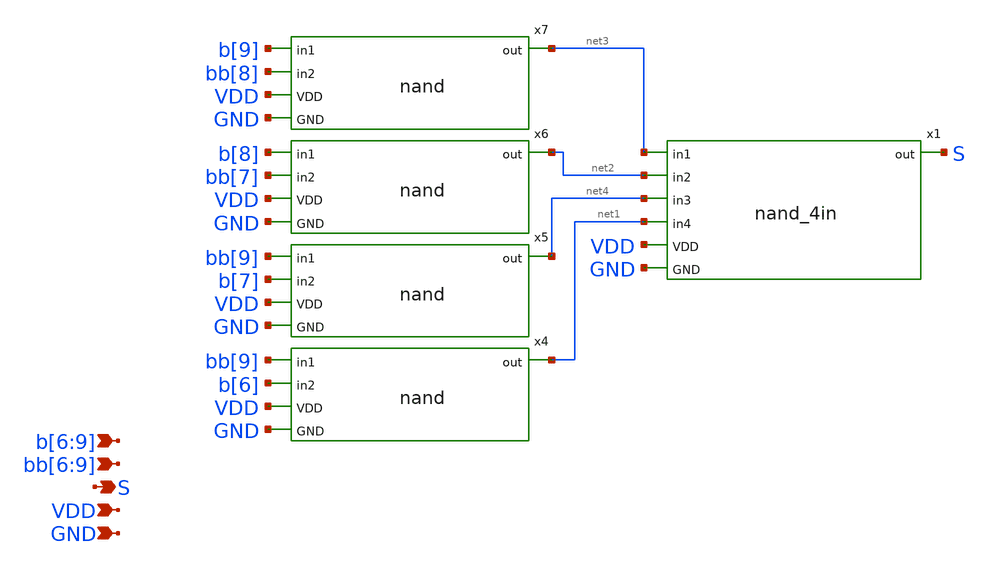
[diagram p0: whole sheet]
** sch_path: xschem/seg_selector_2_logic.sch
**.subckt seg_selector_2_logic b[6],b[7],b[8],b[9] S GND VDD bb[6],bb[7],bb[8],bb[9]
*.ipin b[6],b[7],b[8],b[9]
*.opin S
*.ipin GND
*.ipin VDD
*.ipin bb[6],bb[7],bb[8],bb[9]
x4 bb[9] b[6] net1 VDD GND nand
x5 bb[9] b[7] net4 VDD GND nand
x6 b[8] bb[7] net2 VDD GND nand
x7 b[9] bb[8] net3 VDD GND nand
x1 net3 net2 net4 net1 S VDD GND nand_4in
**.ends

* expanding   symbol:  nand.sym # of pins=5
** sym_path: xschem/nand.sym
** sch_path: xschem/nand.sch
.subckt nand in1 in2 out VDD GND
*.ipin in2
*.opin out
*.ipin VDD
*.ipin GND
*.ipin in1
.param wp=0.63 wn=0.42 l=0.15
XM1 out in1 VDD VDD sky130_fd_pr__pfet_01v8 L=l W=wp nf=1 ad='int((nf+1)/2) * W/nf * 0.29' as='int((nf+2)/2) * W/nf * 0.29'
+ pd='2*int((nf+1)/2) * (W/nf + 0.29)' ps='2*int((nf+2)/2) * (W/nf + 0.29)' nrd='0.29 / W' nrs='0.29 / W'
+ sa=0 sb=0 sd=0 mult=1 m=1
XM2 out in2 VDD VDD sky130_fd_pr__pfet_01v8 L=l W=wp nf=1 ad='int((nf+1)/2) * W/nf * 0.29' as='int((nf+2)/2) * W/nf * 0.29'
+ pd='2*int((nf+1)/2) * (W/nf + 0.29)' ps='2*int((nf+2)/2) * (W/nf + 0.29)' nrd='0.29 / W' nrs='0.29 / W'
+ sa=0 sb=0 sd=0 mult=1 m=1
XM3 out in2 net1 GND sky130_fd_pr__nfet_01v8 L=l W=wn nf=1 ad='int((nf+1)/2) * W/nf * 0.29' as='int((nf+2)/2) * W/nf * 0.29'
+ pd='2*int((nf+1)/2) * (W/nf + 0.29)' ps='2*int((nf+2)/2) * (W/nf + 0.29)' nrd='0.29 / W' nrs='0.29 / W'
+ sa=0 sb=0 sd=0 mult=1 m=1
XM4 net1 in1 GND GND sky130_fd_pr__nfet_01v8 L=l W=wn nf=1 ad='int((nf+1)/2) * W/nf * 0.29' as='int((nf+2)/2) * W/nf * 0.29'
+ pd='2*int((nf+1)/2) * (W/nf + 0.29)' ps='2*int((nf+2)/2) * (W/nf + 0.29)' nrd='0.29 / W' nrs='0.29 / W'
+ sa=0 sb=0 sd=0 mult=1 m=1
.ends


* expanding   symbol:  nand_4in.sym # of pins=7
** sym_path: xschem/nand_4in.sym
** sch_path: xschem/nand_4in.sch
.subckt nand_4in in1 in2 in3 in4 out VDD GND
*.ipin in2
*.opin out
*.ipin VDD
*.ipin GND
*.ipin in1
*.ipin in4
*.ipin in3
.param wp=0.42 wn=0.42 l=0.15
XM1 out in1 VDD VDD sky130_fd_pr__pfet_01v8 L=l W=wp nf=1 ad='int((nf+1)/2) * W/nf * 0.29' as='int((nf+2)/2) * W/nf * 0.29'
+ pd='2*int((nf+1)/2) * (W/nf + 0.29)' ps='2*int((nf+2)/2) * (W/nf + 0.29)' nrd='0.29 / W' nrs='0.29 / W'
+ sa=0 sb=0 sd=0 mult=1 m=1
XM2 out in2 VDD VDD sky130_fd_pr__pfet_01v8 L=l W=wp nf=1 ad='int((nf+1)/2) * W/nf * 0.29' as='int((nf+2)/2) * W/nf * 0.29'
+ pd='2*int((nf+1)/2) * (W/nf + 0.29)' ps='2*int((nf+2)/2) * (W/nf + 0.29)' nrd='0.29 / W' nrs='0.29 / W'
+ sa=0 sb=0 sd=0 mult=1 m=1
XM3 out in1 net1 GND sky130_fd_pr__nfet_01v8 L=l W=wn nf=1 ad='int((nf+1)/2) * W/nf * 0.29' as='int((nf+2)/2) * W/nf * 0.29'
+ pd='2*int((nf+1)/2) * (W/nf + 0.29)' ps='2*int((nf+2)/2) * (W/nf + 0.29)' nrd='0.29 / W' nrs='0.29 / W'
+ sa=0 sb=0 sd=0 mult=1 m=1
XM4 net1 in2 net2 GND sky130_fd_pr__nfet_01v8 L=l W=wn nf=1 ad='int((nf+1)/2) * W/nf * 0.29' as='int((nf+2)/2) * W/nf * 0.29'
+ pd='2*int((nf+1)/2) * (W/nf + 0.29)' ps='2*int((nf+2)/2) * (W/nf + 0.29)' nrd='0.29 / W' nrs='0.29 / W'
+ sa=0 sb=0 sd=0 mult=1 m=1
XM5 out in3 VDD VDD sky130_fd_pr__pfet_01v8 L=l W=wp nf=1 ad='int((nf+1)/2) * W/nf * 0.29' as='int((nf+2)/2) * W/nf * 0.29'
+ pd='2*int((nf+1)/2) * (W/nf + 0.29)' ps='2*int((nf+2)/2) * (W/nf + 0.29)' nrd='0.29 / W' nrs='0.29 / W'
+ sa=0 sb=0 sd=0 mult=1 m=1
XM6 out in4 VDD VDD sky130_fd_pr__pfet_01v8 L=l W=wp nf=1 ad='int((nf+1)/2) * W/nf * 0.29' as='int((nf+2)/2) * W/nf * 0.29'
+ pd='2*int((nf+1)/2) * (W/nf + 0.29)' ps='2*int((nf+2)/2) * (W/nf + 0.29)' nrd='0.29 / W' nrs='0.29 / W'
+ sa=0 sb=0 sd=0 mult=1 m=1
XM7 net2 in3 net3 GND sky130_fd_pr__nfet_01v8 L=l W=wn nf=1 ad='int((nf+1)/2) * W/nf * 0.29' as='int((nf+2)/2) * W/nf * 0.29'
+ pd='2*int((nf+1)/2) * (W/nf + 0.29)' ps='2*int((nf+2)/2) * (W/nf + 0.29)' nrd='0.29 / W' nrs='0.29 / W'
+ sa=0 sb=0 sd=0 mult=1 m=1
XM8 net3 in4 GND GND sky130_fd_pr__nfet_01v8 L=l W=wn nf=1 ad='int((nf+1)/2) * W/nf * 0.29' as='int((nf+2)/2) * W/nf * 0.29'
+ pd='2*int((nf+1)/2) * (W/nf + 0.29)' ps='2*int((nf+2)/2) * (W/nf + 0.29)' nrd='0.29 / W' nrs='0.29 / W'
+ sa=0 sb=0 sd=0 mult=1 m=1
.ends

.end
